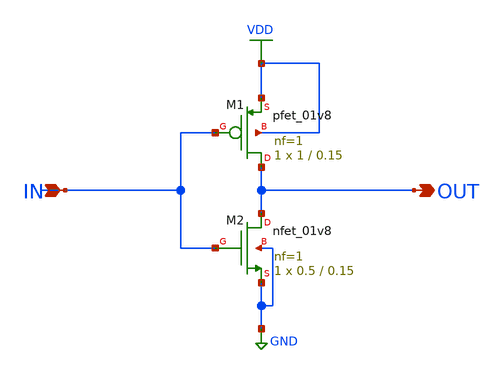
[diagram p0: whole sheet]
** sch_path: in.sch
**.subckt in OUT IN
*.opin OUT
*.ipin IN
XM1 OUT IN VDD VDD sky130_fd_pr__pfet_01v8 L=0.15 W=1 nf=1 ad='int((nf+1)/2) * W/nf * 0.29' as='int((nf+2)/2) * W/nf * 0.29'
+ pd='2*int((nf+1)/2) * (W/nf + 0.29)' ps='2*int((nf+2)/2) * (W/nf + 0.29)' nrd='0.29 / W' nrs='0.29 / W'
+ sa=0 sb=0 sd=0 mult=1 m=1
XM2 OUT IN GND GND sky130_fd_pr__nfet_01v8 L=0.15 W=0.5 nf=1 ad='int((1 + 1)/2) * 0.5 / 1 * 0.29' as='int((1 + 2)/2) * 0.5 / 1 * 0.29'
+ pd='2*int((1 + 1)/2) * (0.5 / 1 + 0.29)' ps='2*int((1 + 2)/2) * (0.5 / 1 + 0.29)' nrd='0.29 / 0.5 ' nrs='0.29 / 0.5 '
+ sa=0 sb=0 sd=0 mult=1 m=1
**.ends
.GLOBAL GND
.GLOBAL VDD
.end
